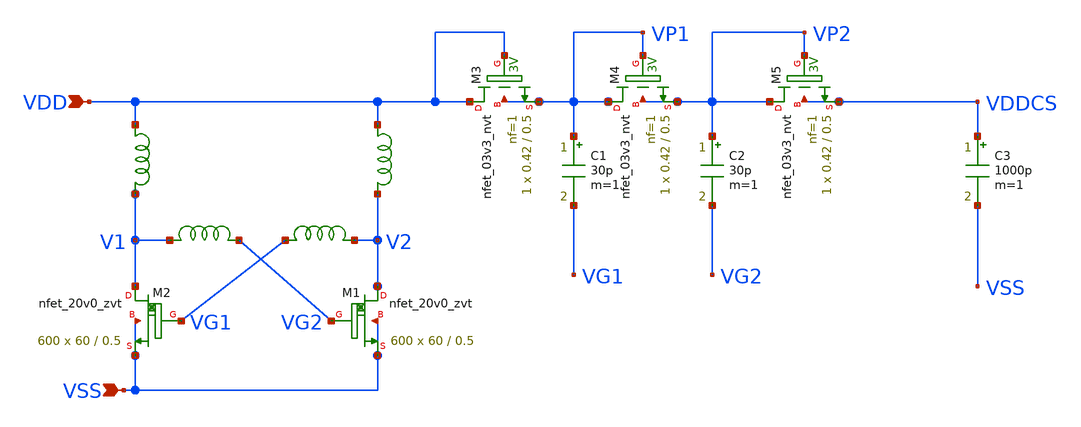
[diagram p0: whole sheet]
** sch_path: design/LELO_SVOD_SKY130A/LELO_EXSC.sch
**.subckt LELO_EXSC VSS VDD
*.ipin VSS
*.ipin VDD
C1 VP1 VG1 30p m=1
C2 VP2 VG2 30p m=1
XM3 VDD VDD VP1 VP1 sky130_fd_pr__nfet_03v3_nvt L=0.5 W=0.42 nf=1 ad='int((1 + 1)/2) * 0.42 / 1 * 0.29'
+ as='int((1 + 2)/2) * 0.42 / 1 * 0.29' pd='2*int((1 + 1)/2) * (0.42 / 1 + 0.29)' ps='2*int((1 + 2)/2) * (0.42 / 1 + 0.29)'
+ nrd='0.29 / 0.42 ' nrs='0.29 / 0.42 ' sa=0 sb=0 sd=0 mult=1 m=1
x3 VDD V2 1812PS-102_imp
x4 VDD V1 1812PS-102_imp
XM1 V2 VG2 VSS VSS sky130_fd_pr__nfet_20v0_zvt W=60 L=0.5 m=600
XM2 V1 VG1 VSS VSS sky130_fd_pr__nfet_20v0_zvt W=60 L=0.5 m=600
XM4 VP1 VP1 VP2 VP2 sky130_fd_pr__nfet_03v3_nvt L=0.5 W=0.42 nf=1 ad='int((1 + 1)/2) * 0.42 / 1 * 0.29'
+ as='int((1 + 2)/2) * 0.42 / 1 * 0.29' pd='2*int((1 + 1)/2) * (0.42 / 1 + 0.29)' ps='2*int((1 + 2)/2) * (0.42 / 1 + 0.29)'
+ nrd='0.29 / 0.42 ' nrs='0.29 / 0.42 ' sa=0 sb=0 sd=0 mult=1 m=1
XM5 VP2 VP2 VDDCS VDDCS sky130_fd_pr__nfet_03v3_nvt L=0.5 W=0.42 nf=1 ad='int((1 + 1)/2) * 0.42 / 1 * 0.29'
+ as='int((1 + 2)/2) * 0.42 / 1 * 0.29' pd='2*int((1 + 1)/2) * (0.42 / 1 + 0.29)' ps='2*int((1 + 2)/2) * (0.42 / 1 + 0.29)'
+ nrd='0.29 / 0.42 ' nrs='0.29 / 0.42 ' sa=0 sb=0 sd=0 mult=1 m=1
C3 VDDCS VSS 1000p m=1
x1 V1 VG2 1812PS-473_imp
x2 VG1 V2 1812PS-473_imp
**.ends

* expanding   symbol:  LELO_SVOD_SKY130A/1812PS-102_imp.sym # of pins=2
** sym_path: design/LELO_SVOD_SKY130A/1812PS-102_imp.sym

.subckt 1812PS-102_imp port1 port2
X1 port1 port2 Model1D R1=60 R2=0.054 C= 0.15p K1=0.000001 K2=0.064 K3= 1u K4=1E-06 K5=0.000001 L=0
+ Is=0 a=0 L_Z0=0 L_EL=0 L_F0=0E6 PkZ=1282.46492
.ends 1812PS-102_imp

* expanding   symbol:  LELO_SVOD_SKY130A/1812PS-473_imp.sym # of pins=2
** sym_path: design/LELO_SVOD_SKY130A/1812PS-473_imp.sym

.subckt 1812PS-473_imp port1 port2
X1 port1 port2 Model1D R1=30 R2=0.87 C= 0.767p K1=0.000001 K2=4.63 K3= 47u K4=0.647 K5=0.00000972
+ L=0 Is=0 a=0 L_Z0=0 L_EL=0 L_F0=0E6 PkZ=23517.1382
.ends 1812PS-473_imp
.end
